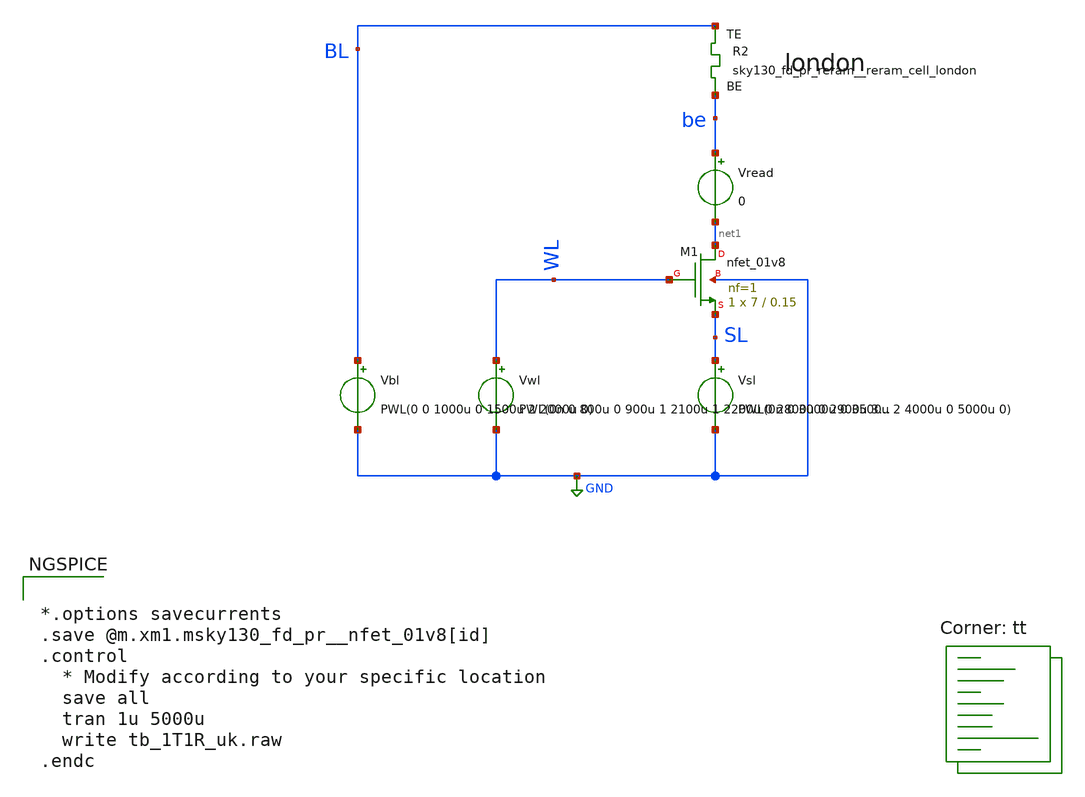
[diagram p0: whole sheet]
** sch_path: memristor_models/rram_london/tb_1T1R_uk.sch
**.subckt tb_1T1R_uk
XM1 net1 WL SL GND sky130_fd_pr__nfet_01v8 L=0.15 W=7 nf=1 ad='int((nf+1)/2) * W/nf * 0.29' as='int((nf+2)/2) * W/nf * 0.29'
+ pd='2*int((nf+1)/2) * (W/nf + 0.29)' ps='2*int((nf+2)/2) * (W/nf + 0.29)' nrd='0.29 / W' nrs='0.29 / W'
+ sa=0 sb=0 sd=0 mult=1 m=1
Vwl WL GND PWL(0n 0 800u 0 900u 1 2100u 1 2200u 0 2800u 0 2900u 3 4100u 3 4200u 0 5000u 0)
Vbl BL GND PWL(0 0 1000u 0 1500u 2 2000u 0)
Vsl SL GND PWL(0n 0 3000u 0 3500u 2 4000u 0 5000u 0)
XR2 BL be sky130_fd_pr_reram__reram_cell_london
Vread be net1 0
**** begin user architecture code


*.options savecurrents
.save @m.xm1.msky130_fd_pr__nfet_01v8[id]
.control
  * Modify according to your specific location
  save all
  tran 1u 5000u
  write tb_1T1R_uk.raw
.endc



.lib $::SKYWATER_MODELS/sky130.lib.spice tt

** opencircuitdesign pdks install
.inc $::SKYWATER_MODELS/sky130_fd_pr_reram__reram_cell_london.spice

**** end user architecture code
**.ends
.GLOBAL GND
.end
